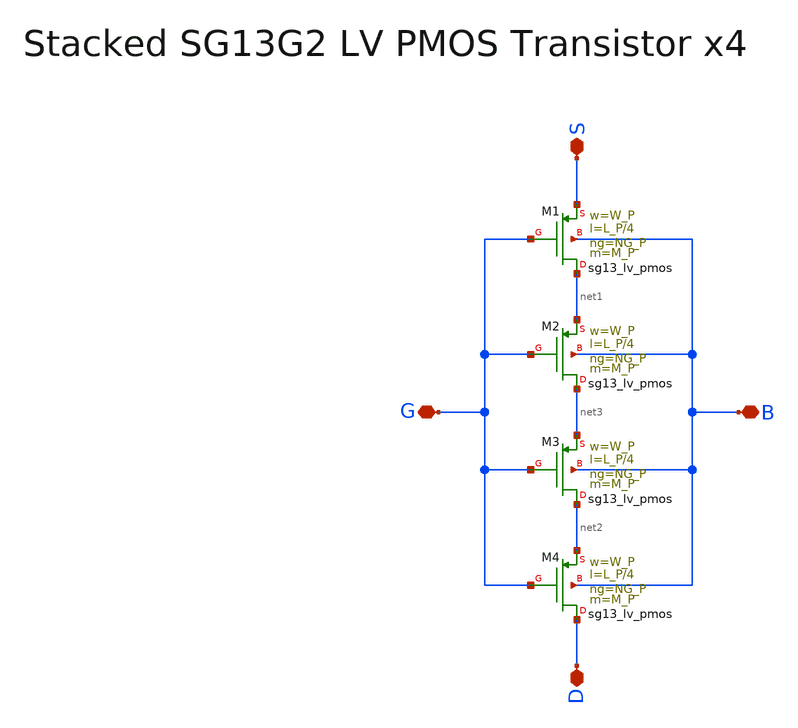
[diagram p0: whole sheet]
** sch_path: SG13G2_ATBS-ADC-main/xschem/stacked_transistors/sg13g2_lv_pmos_stacked/sg13g2_lv_pmos_stacked_x4.sch
**.subckt sg13g2_lv_pmos_stacked_x4 D S G B
*.iopin D
*.iopin S
*.iopin G
*.iopin B
XM1 net1 G S B sg13_lv_pmos w=W_P l=L_P/4 ng=NG_P m=M_P mm_ok=1
XM2 net3 G net1 B sg13_lv_pmos w=W_P l=L_P/4 ng=NG_P m=M_P mm_ok=1
XM3 net2 G net3 B sg13_lv_pmos w=W_P l=L_P/4 ng=NG_P m=M_P mm_ok=1
XM4 D G net2 B sg13_lv_pmos w=W_P l=L_P/4 ng=NG_P m=M_P mm_ok=1
**.ends
.end
